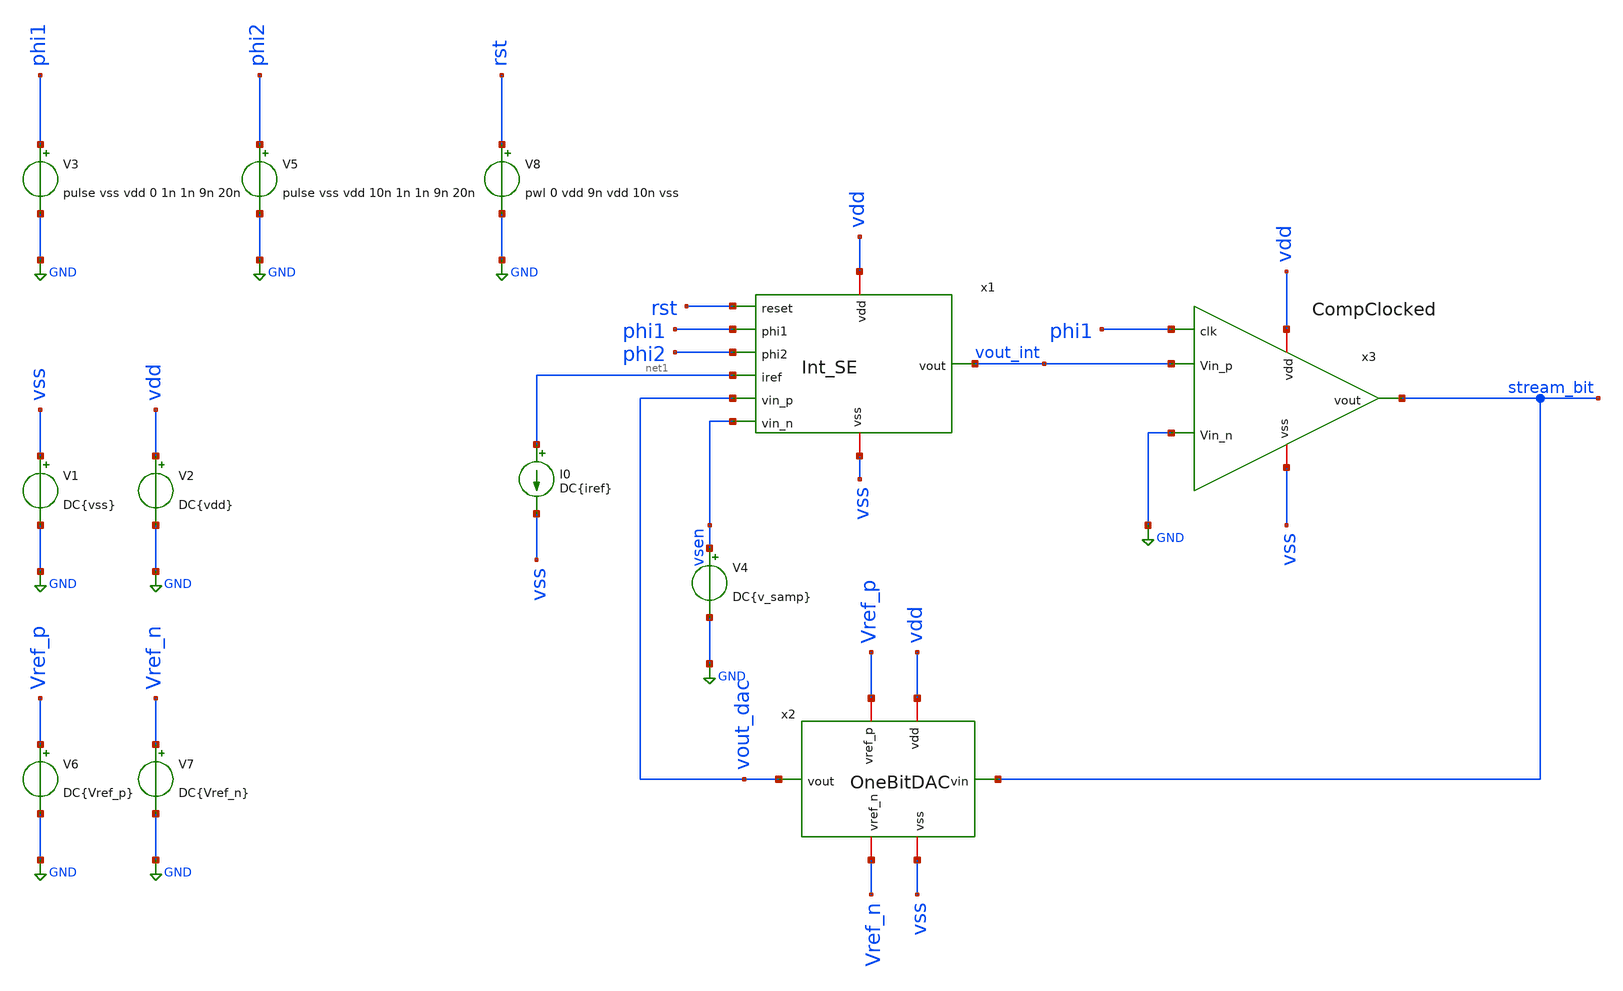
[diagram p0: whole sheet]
** sch_path: xschem/SigmaDelta_tb.sch

.lib $::SKYWATER_MODELS/sky130.lib.spice tt
.include $::SKYWATER_STDCELLS/sky130_fd_sc_hd.spice

**.subckt SigmaDelta_tb
V1 vss GND DC{vss}
V2 vdd GND DC{vdd}
I0 net1 vss DC{iref}
V3 phi1 GND pulse vss vdd 0 1n 1n 9n 20n
V5 phi2 GND pulse vss vdd 10n 1n 1n 9n 20n
x2 Vref_p vdd stream_bit vout_dac Vref_n vss OneBitDAC
V6 Vref_p GND DC{Vref_p}
V7 Vref_n GND DC{Vref_n}
x1 rst phi1 vdd vsen vout_int net1 phi2 vss vout_dac Int_SE
x3 vdd phi1 stream_bit GND vout_int vss CompClocked
V8 rst GND pwl 0 vdd 9n vdd 10n vss
V4 vsen GND DC{v_samp}
**** begin user architecture code

* this option enables mos model bin
* selection based on W/NF instead of W
.option wnflag=1
.option savecurrents

* Circuit Parameters
.param iref = 100u
.param vdd  = 1.8
.param vss  = -1.8
.param Vref_p = 1.5
.param Vref_n = -1.5
.param v_samp = 0.3
.options TEMP = 25.0
* Comp param
.param Wn = 3
.param Wp = 3

* OP Parameters & Singals to save
.save all

*Simulations
.control
  save v(x2.VINV) v(x1.vc1) v(x2.vc2) v(x3.vcomp_n)
  tran 0.1n 300n
  setplot tran1
  plot v(vsen) v(vout_Int) v(phi1) v(phi2) v(vout_dac)
  plot v(x1.vc1) - v(x1.vc2)
  plot v(x3.vcomp_n)
  write /foss/designs/SigmaDelta_ADC/xschem/sim_results/SigmaDelta.raw
.endc

.end


**** end user architecture code
**.ends
.GLOBAL GND
.end
